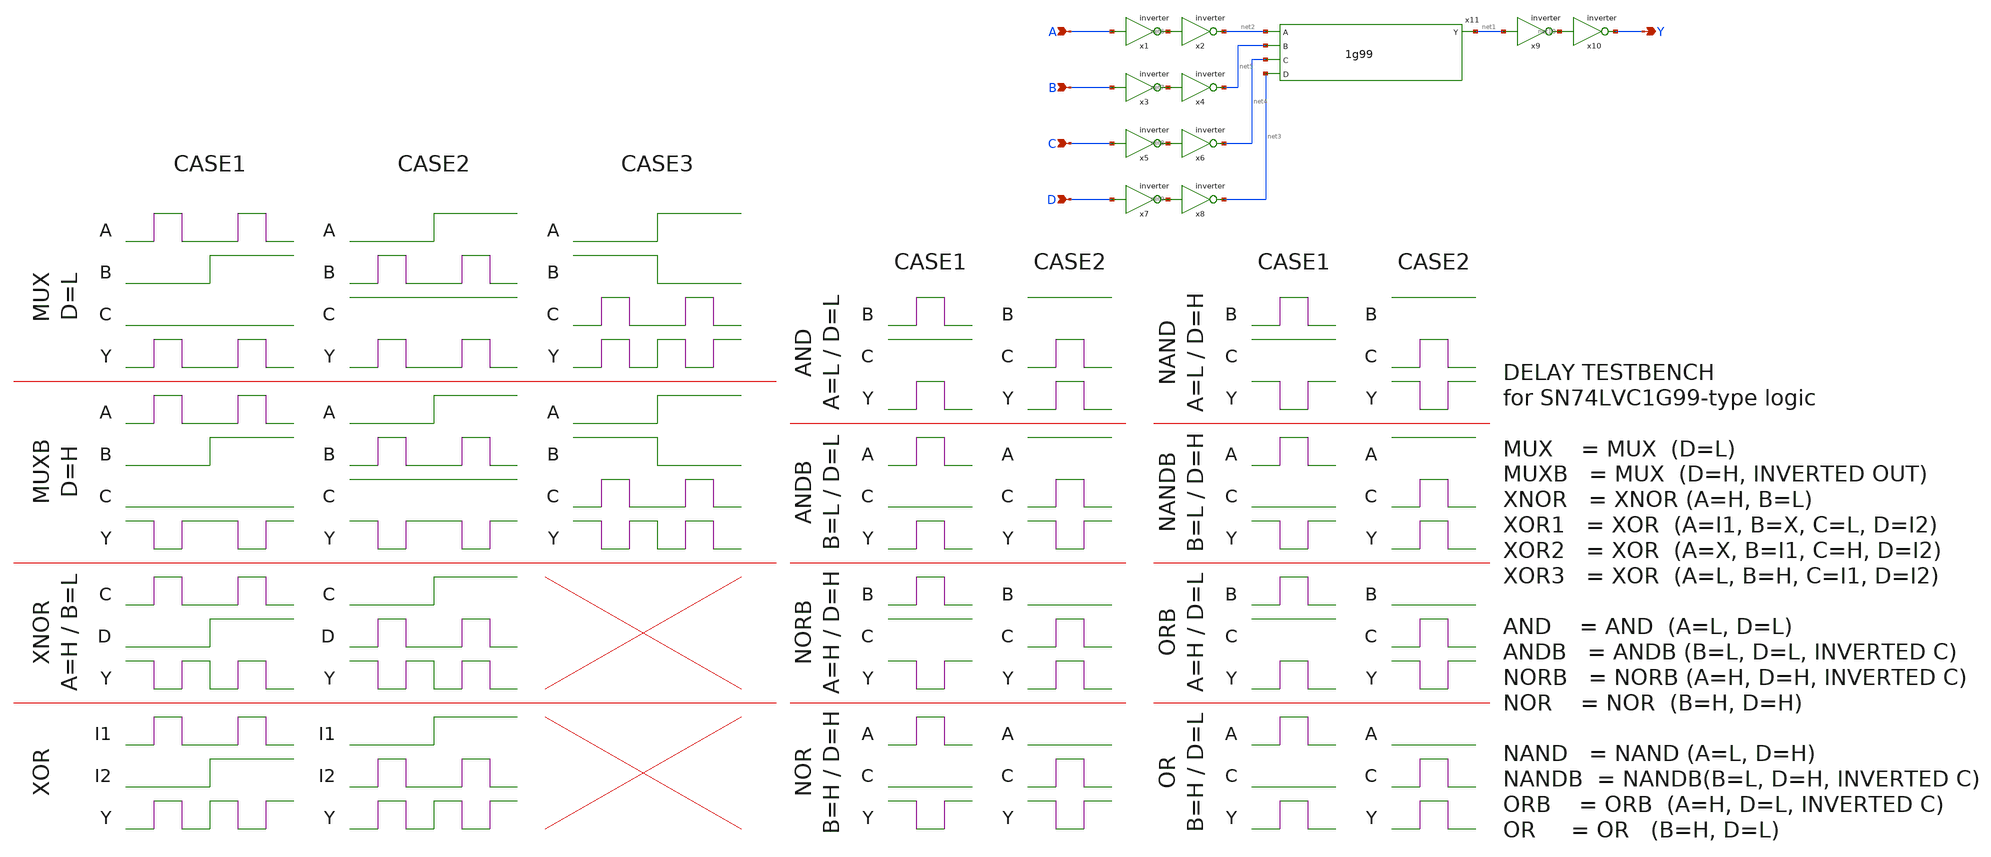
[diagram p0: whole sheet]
** sch_path: 1g99_delay2.sch
**.subckt 1g99_delay2 A B C D Y
*.ipin A
*.ipin B
*.ipin C
*.ipin D
*.opin Y
x1 net6 A inverter
x2 net2 net6 inverter
x3 net7 B inverter
x4 net5 net7 inverter
x5 net8 C inverter
x6 net4 net8 inverter
x7 net9 D inverter
x8 net3 net9 inverter
x9 net10 net1 inverter
x10 Y net10 inverter
x11 net2 net5 net1 net4 net3 1g99
**** begin user architecture code
 .param mc_mm_switch=0
.param mc_pr_switch=0
.include $::SKYWATER_MODELS/corners/tt.spice
.include $::SKYWATER_MODELS/r+c/res_typical__cap_typical.spice
.include $::SKYWATER_MODELS/r+c/res_typical__cap_typical__lin.spice
.include $::SKYWATER_MODELS/corners/tt/specialized_cells.spice
.include $::SKYWATER_STDCELLS/sky130_fd_sc_hd.spice




VP VDD 0 dc 1.8
VA A 0 dc 1.8
VB B 0 dc 1.8
VC C 0 dc 1.8
VD D 0 dc 1.8

.control
save a b c d y

// MUX AREA

alter @vd[PULSE] [ 0 0 10n 40p 40p 10n 30n ] // always L

alter @va[PULSE] [ 0 1.8 10n 40p 40p 10n 30n ]
alter @vb[PULSE] [ 0 1.8 30n 40p 40p 40n 80n ]
alter @vc[PULSE] [ 0 0 10n 40p 40p 10n 30n ]
tran 10p 60n
meas tran  in1 FIND time WHEN v(a)=0.9 RISE=1 > NUL
meas tran out1 FIND time WHEN v(y)=0.9 RISE=1 > NUL
meas tran  in2 FIND time WHEN v(a)=0.9 FALL=1 > NUL
meas tran out2 FIND time WHEN v(y)=0.9 FALL=1 > NUL
meas tran  in3 FIND time WHEN v(a)=0.9 RISE=2 > NUL
meas tran out3 FIND time WHEN v(y)=0.9 RISE=2 > NUL
meas tran  in4 FIND time WHEN v(a)=0.9 FALL=2 > NUL
meas tran out4 FIND time WHEN v(y)=0.9 FALL=2 > NUL

let calc1 = out1 - in1
set delay1 = $&calc1
let calc2 = out2 - in2
set delay2 = $&calc2
let calc3 = out3 - in3
set delay3 = $&calc3
let calc4 = out4 - in4
set delay4 = $&calc4

alter @vb[PULSE] [ 0 1.8 10n 40p 40p 10n 30n ]
alter @va[PULSE] [ 0 1.8 30n 40p 40p 40n 80n ]
alter @vc[PULSE] [ 1.8 1.8 10n 40p 40p 10n 30n ]
tran 10p 60n
meas tran  in5 FIND time WHEN v(b)=0.9 RISE=1 > NUL
meas tran out5 FIND time WHEN v(y)=0.9 RISE=1 > NUL
meas tran  in6 FIND time WHEN v(b)=0.9 FALL=1 > NUL
meas tran out6 FIND time WHEN v(y)=0.9 FALL=1 > NUL
meas tran  in7 FIND time WHEN v(b)=0.9 RISE=2 > NUL
meas tran out7 FIND time WHEN v(y)=0.9 RISE=2 > NUL
meas tran  in8 FIND time WHEN v(b)=0.9 FALL=2 > NUL
meas tran out8 FIND time WHEN v(y)=0.9 FALL=2 > NUL

let calc5 = out5 - in5
set delay5 = $&calc5
let calc6 = out6 - in6
set delay6 = $&calc6
let calc7 = out7 - in7
set delay7 = $&calc7
let calc8 = out8 - in8
set delay8 = $&calc8

alter @va[PULSE] [ 0 1.8 30n 40p 40p 40n 80n ]
alter @vb[PULSE] [ 1.8 0 30n 40p 40p 40n 80n ]
alter @vc[PULSE] [ 0 1.8 10n 40p 40p 10n 30n ]
tran 10p 60n
meas tran  in9 FIND time WHEN v(c)=0.9 RISE=1 > NUL
meas tran out9 FIND time WHEN v(y)=0.9 RISE=1 > NUL
meas tran  in10 FIND time WHEN v(c)=0.9 FALL=1 > NUL
meas tran out10 FIND time WHEN v(y)=0.9 FALL=1 > NUL
meas tran  in11 FIND time WHEN v(c)=0.9 RISE=2 > NUL
meas tran out11 FIND time WHEN v(y)=0.9 FALL=2 > NUL
meas tran  in12 FIND time WHEN v(c)=0.9 FALL=2 > NUL
meas tran out12 FIND time WHEN v(y)=0.9 RISE=3 > NUL

let calc9 = out9 - in9
set delay9 = $&calc9
let calc10 = out10 - in10
set delay10 = $&calc10
let calc11 = out11 - in11
set delay11 = $&calc11
let calc12 = out12 - in12
set delay12 = $&calc12

// MUXB AREA

alter @vd[PULSE] [ 1.8 1.8 10n 40p 40p 10n 30n ] // always H

alter @va[PULSE] [ 0 1.8 10n 40p 40p 10n 30n ]
alter @vb[PULSE] [ 0 1.8 30n 40p 40p 40n 80n ]
alter @vc[PULSE] [ 0 0 10n 40p 40p 10n 30n ]
tran 10p 60n
meas tran  in1 FIND time WHEN v(a)=0.9 RISE=1 > NUL
meas tran out1 FIND time WHEN v(y)=0.9 FALL=1 > NUL
meas tran  in2 FIND time WHEN v(a)=0.9 FALL=1 > NUL
meas tran out2 FIND time WHEN v(y)=0.9 RISE=1 > NUL
meas tran  in3 FIND time WHEN v(a)=0.9 RISE=2 > NUL
meas tran out3 FIND time WHEN v(y)=0.9 FALL=2 > NUL
meas tran  in4 FIND time WHEN v(a)=0.9 FALL=2 > NUL
meas tran out4 FIND time WHEN v(y)=0.9 RISE=2 > NUL

let calc1 = out1 - in1
set delayb1 = $&calc1
let calc2 = out2 - in2
set delayb2 = $&calc2
let calc3 = out3 - in3
set delayb3 = $&calc3
let calc4 = out4 - in4
set delayb4 = $&calc4

alter @vb[PULSE] [ 0 1.8 10n 40p 40p 10n 30n ]
alter @va[PULSE] [ 0 1.8 30n 40p 40p 40n 80n ]
alter @vc[PULSE] [ 1.8 1.8 10n 40p 40p 10n 30n ]
tran 10p 60n
meas tran  in5 FIND time WHEN v(b)=0.9 RISE=1 > NUL
meas tran out5 FIND time WHEN v(y)=0.9 FALL=1 > NUL
meas tran  in6 FIND time WHEN v(b)=0.9 FALL=1 > NUL
meas tran out6 FIND time WHEN v(y)=0.9 RISE=1 > NUL
meas tran  in7 FIND time WHEN v(b)=0.9 RISE=2 > NUL
meas tran out7 FIND time WHEN v(y)=0.9 FALL=2 > NUL
meas tran  in8 FIND time WHEN v(b)=0.9 FALL=2 > NUL
meas tran out8 FIND time WHEN v(y)=0.9 RISE=2 > NUL

let calc5 = out5 - in5
set delayb5 = $&calc5
let calc6 = out6 - in6
set delayb6 = $&calc6
let calc7 = out7 - in7
set delayb7 = $&calc7
let calc8 = out8 - in8
set delayb8 = $&calc8

alter @va[PULSE] [ 0 1.8 30n 40p 40p 40n 80n ]
alter @vb[PULSE] [ 1.8 0 30n 40p 40p 40n 80n ]
alter @vc[PULSE] [ 0 1.8 10n 40p 40p 10n 30n ]
tran 10p 60n
meas tran  in9 FIND time WHEN v(c)=0.9 RISE=1 > NUL
meas tran out9 FIND time WHEN v(y)=0.9 FALL=1 > NUL
meas tran  in10 FIND time WHEN v(c)=0.9 FALL=1 > NUL
meas tran out10 FIND time WHEN v(y)=0.9 RISE=1 > NUL
meas tran  in11 FIND time WHEN v(c)=0.9 RISE=2 > NUL
meas tran out11 FIND time WHEN v(y)=0.9 RISE=2 > NUL
meas tran  in12 FIND time WHEN v(c)=0.9 FALL=2 > NUL
meas tran out12 FIND time WHEN v(y)=0.9 FALL=3 > NUL

let calc9 = out9 - in9
set delayb9 = $&calc9
let calc10 = out10 - in10
set delayb10 = $&calc10
let calc11 = out11 - in11
set delayb11 = $&calc11
let calc12 = out12 - in12
set delayb12 = $&calc12

// XNOR AREA

alter @va[PULSE] [ 1.8 1.8 30n 40p 40p 10n 30n ] // always H
alter @vb[PULSE] [ 0 0 30n 40p 40p 10n 30n ] // always L
alter @vc[PULSE] [ 0 1.8 10n 40p 40p 10n 30n ]
alter @vd[PULSE] [ 0 1.8 30n 40p 40p 40n 80n ]
tran 10p 60n
meas tran  in1 FIND time WHEN v(c)=0.9 RISE=1 > NUL
meas tran out1 FIND time WHEN v(y)=0.9 FALL=1 > NUL
meas tran  in2 FIND time WHEN v(c)=0.9 FALL=1 > NUL
meas tran out2 FIND time WHEN v(y)=0.9 RISE=1 > NUL
meas tran  in3 FIND time WHEN v(c)=0.9 RISE=2 > NUL
meas tran out3 FIND time WHEN v(y)=0.9 RISE=2 > NUL
meas tran  in4 FIND time WHEN v(c)=0.9 FALL=2 > NUL
meas tran out4 FIND time WHEN v(y)=0.9 FALL=3 > NUL

let calc1 = out1 - in1
set delayxn1 = $&calc1
let calc2 = out2 - in2
set delayxn2 = $&calc2
let calc3 = out3 - in3
set delayxn3 = $&calc3
let calc4 = out4 - in4
set delayxn4 = $&calc4

alter @vd[PULSE] [ 0 1.8 10n 40p 40p 10n 30n ]
alter @vc[PULSE] [ 0 1.8 30n 40p 40p 40n 80n ]
tran 10p 60n
meas tran  in5 FIND time WHEN v(d)=0.9 RISE=1 > NUL
meas tran out5 FIND time WHEN v(y)=0.9 FALL=1 > NUL
meas tran  in6 FIND time WHEN v(d)=0.9 FALL=1 > NUL
meas tran out6 FIND time WHEN v(y)=0.9 RISE=1 > NUL
meas tran  in7 FIND time WHEN v(d)=0.9 RISE=2 > NUL
meas tran out7 FIND time WHEN v(y)=0.9 RISE=2 > NUL
meas tran  in8 FIND time WHEN v(d)=0.9 FALL=2 > NUL
meas tran out8 FIND time WHEN v(y)=0.9 FALL=3 > NUL

let calc5 = out5 - in5
set delayxn5 = $&calc5
let calc6 = out6 - in6
set delayxn6 = $&calc6
let calc7 = out7 - in7
set delayxn7 = $&calc7
let calc8 = out8 - in8
set delayxn8 = $&calc8

// XOR_A AREA

alter @vb[PULSE] [ 0 0 10n 40p 40p 10n 30n ] // assume L
alter @vc[PULSE] [ 0 0 10n 40p 40p 10n 30n ] // always L

alter @va[PULSE] [ 0 1.8 10n 40p 40p 10n 30n ]
alter @vd[PULSE] [ 0 1.8 30n 40p 40p 40n 80n ]
tran 10p 60n
meas tran  in1 FIND time WHEN v(a)=0.9 RISE=1 > NUL
meas tran out1 FIND time WHEN v(y)=0.9 RISE=1 > NUL
meas tran  in2 FIND time WHEN v(a)=0.9 FALL=1 > NUL
meas tran out2 FIND time WHEN v(y)=0.9 FALL=1 > NUL
meas tran  in3 FIND time WHEN v(a)=0.9 RISE=2 > NUL
meas tran out3 FIND time WHEN v(y)=0.9 FALL=2 > NUL
meas tran  in4 FIND time WHEN v(a)=0.9 FALL=2 > NUL
meas tran out4 FIND time WHEN v(y)=0.9 RISE=3 > NUL

let calc1 = out1 - in1
set delayxa1 = $&calc1
let calc2 = out2 - in2
set delayxa2 = $&calc2
let calc3 = out3 - in3
set delayxa3 = $&calc3
let calc4 = out4 - in4
set delayxa4 = $&calc4

alter @vd[PULSE] [ 0 1.8 10n 40p 40p 10n 30n ]
alter @va[PULSE] [ 0 1.8 30n 40p 40p 40n 80n ]
tran 10p 60n
meas tran  in5 FIND time WHEN v(d)=0.9 RISE=1 > NUL
meas tran out5 FIND time WHEN v(y)=0.9 RISE=1 > NUL
meas tran  in6 FIND time WHEN v(d)=0.9 FALL=1 > NUL
meas tran out6 FIND time WHEN v(y)=0.9 FALL=1 > NUL
meas tran  in7 FIND time WHEN v(d)=0.9 RISE=2 > NUL
meas tran out7 FIND time WHEN v(y)=0.9 FALL=2 > NUL
meas tran  in8 FIND time WHEN v(d)=0.9 FALL=2 > NUL
meas tran out8 FIND time WHEN v(y)=0.9 RISE=3 > NUL

let calc5 = out5 - in5
set delayxa5 = $&calc5
let calc6 = out6 - in6
set delayxa6 = $&calc6
let calc7 = out7 - in7
set delayxa7 = $&calc7
let calc8 = out8 - in8
set delayxa8 = $&calc8

// XOR_B AREA

alter @va[PULSE] [ 0 0 10n 40p 40p 10n 30n ]     // assume L
alter @vc[PULSE] [ 1.8 1.8 10n 40p 40p 10n 30n ] // always H

alter @vb[PULSE] [ 0 1.8 10n 40p 40p 10n 30n ]
alter @vd[PULSE] [ 0 1.8 30n 40p 40p 40n 80n ]
tran 10p 60n
meas tran  in1 FIND time WHEN v(b)=0.9 RISE=1 > NUL
meas tran out1 FIND time WHEN v(y)=0.9 RISE=1 > NUL
meas tran  in2 FIND time WHEN v(b)=0.9 FALL=1 > NUL
meas tran out2 FIND time WHEN v(y)=0.9 FALL=1 > NUL
meas tran  in3 FIND time WHEN v(b)=0.9 RISE=2 > NUL
meas tran out3 FIND time WHEN v(y)=0.9 FALL=2 > NUL
meas tran  in4 FIND time WHEN v(b)=0.9 FALL=2 > NUL
meas tran out4 FIND time WHEN v(y)=0.9 RISE=3 > NUL

let calc1 = out1 - in1
set delayxb1 = $&calc1
let calc2 = out2 - in2
set delayxb2 = $&calc2
let calc3 = out3 - in3
set delayxb3 = $&calc3
let calc4 = out4 - in4
set delayxb4 = $&calc4

alter @vd[PULSE] [ 0 1.8 10n 40p 40p 10n 30n ]
alter @vb[PULSE] [ 0 1.8 30n 40p 40p 40n 80n ]
tran 10p 60n
meas tran  in5 FIND time WHEN v(d)=0.9 RISE=1 > NUL
meas tran out5 FIND time WHEN v(y)=0.9 RISE=1 > NUL
meas tran  in6 FIND time WHEN v(d)=0.9 FALL=1 > NUL
meas tran out6 FIND time WHEN v(y)=0.9 FALL=1 > NUL
meas tran  in7 FIND time WHEN v(d)=0.9 RISE=2 > NUL
meas tran out7 FIND time WHEN v(y)=0.9 FALL=2 > NUL
meas tran  in8 FIND time WHEN v(d)=0.9 FALL=2 > NUL
meas tran out8 FIND time WHEN v(y)=0.9 RISE=3 > NUL

let calc5 = out5 - in5
set delayxb5 = $&calc5
let calc6 = out6 - in6
set delayxb6 = $&calc6
let calc7 = out7 - in7
set delayxb7 = $&calc7
let calc8 = out8 - in8
set delayxb8 = $&calc8

//XOR_C AREA

alter @va[PULSE] [ 0 0 10n 40p 40p 10n 30n ]     // assume L
alter @vb[PULSE] [ 1.8 1.8 10n 40p 40p 10n 30n ] // always H

alter @vc[PULSE] [ 0 1.8 10n 40p 40p 10n 30n ]
alter @vd[PULSE] [ 0 1.8 30n 40p 40p 40n 80n ]
tran 10p 60n
meas tran  in1 FIND time WHEN v(c)=0.9 RISE=1 > NUL
meas tran out1 FIND time WHEN v(y)=0.9 RISE=1 > NUL
meas tran  in2 FIND time WHEN v(c)=0.9 FALL=1 > NUL
meas tran out2 FIND time WHEN v(y)=0.9 FALL=1 > NUL
meas tran  in3 FIND time WHEN v(c)=0.9 RISE=2 > NUL
meas tran out3 FIND time WHEN v(y)=0.9 FALL=2 > NUL
meas tran  in4 FIND time WHEN v(c)=0.9 FALL=2 > NUL
meas tran out4 FIND time WHEN v(y)=0.9 RISE=3 > NUL

let calc1 = out1 - in1
set delayxc1 = $&calc1
let calc2 = out2 - in2
set delayxc2 = $&calc2
let calc3 = out3 - in3
set delayxc3 = $&calc3
let calc4 = out4 - in4
set delayxc4 = $&calc4

alter @vd[PULSE] [ 0 1.8 10n 40p 40p 10n 30n ]
alter @vc[PULSE] [ 0 1.8 30n 40p 40p 40n 80n ]
tran 10p 60n
meas tran  in5 FIND time WHEN v(d)=0.9 RISE=1 > NUL
meas tran out5 FIND time WHEN v(y)=0.9 RISE=1 > NUL
meas tran  in6 FIND time WHEN v(d)=0.9 FALL=1 > NUL
meas tran out6 FIND time WHEN v(y)=0.9 FALL=1 > NUL
meas tran  in7 FIND time WHEN v(d)=0.9 RISE=2 > NUL
meas tran out7 FIND time WHEN v(y)=0.9 FALL=2 > NUL
meas tran  in8 FIND time WHEN v(d)=0.9 FALL=2 > NUL
meas tran out8 FIND time WHEN v(y)=0.9 RISE=3 > NUL

let calc5 = out5 - in5
set delayxc5 = $&calc5
let calc6 = out6 - in6
set delayxc6 = $&calc6
let calc7 = out7 - in7
set delayxc7 = $&calc7
let calc8 = out8 - in8
set delayxc8 = $&calc8

// AND AREA

alter @va[PULSE] [ 0 0 10n 40p 40p 10n 30n ] // always L
alter @vd[PULSE] [ 0 0 10n 40p 40p 10n 30n ] // always L

alter @vb[PULSE] [ 0 1.8 10n 40p 40p 10n 30n ]
alter @vc[PULSE] [ 1.8 1.8 10n 40p 40p 10n 30n ]
tran 10p 30n
meas tran  in1 FIND time WHEN v(b)=0.9 RISE=1 > NUL
meas tran out1 FIND time WHEN v(y)=0.9 RISE=1 > NUL
meas tran  in2 FIND time WHEN v(b)=0.9 FALL=1 > NUL
meas tran out2 FIND time WHEN v(y)=0.9 FALL=1 > NUL

let calc1 = out1 - in1
set delaya1 = $&calc1
let calc2 = out2 - in2
set delaya2 = $&calc2

alter @vc[PULSE] [ 0 1.8 10n 40p 40p 10n 30n ]
alter @vb[PULSE] [ 1.8 1.8 10n 40p 40p 10n 30n ]
tran 10p 30n
meas tran  in5 FIND time WHEN v(c)=0.9 RISE=1 > NUL
meas tran out5 FIND time WHEN v(y)=0.9 RISE=1 > NUL
meas tran  in6 FIND time WHEN v(c)=0.9 FALL=1 > NUL
meas tran out6 FIND time WHEN v(y)=0.9 FALL=1 > NUL

let calc5 = out5 - in5
set delaya5 = $&calc5
let calc6 = out6 - in6
set delaya6 = $&calc6

// NORB_A AREA

alter @vb[PULSE] [ 0 0 10n 40p 40p 10n 30n ] // always L
alter @vd[PULSE] [ 0 0 10n 40p 40p 10n 30n ] // always L

alter @va[PULSE] [ 0 1.8 10n 40p 40p 10n 30n ]
alter @vc[PULSE] [ 0 0 10n 40p 40p 10n 30n ]
tran 10p 30n
meas tran  in1 FIND time WHEN v(a)=0.9 RISE=1 > NUL
meas tran out1 FIND time WHEN v(y)=0.9 RISE=1 > NUL
meas tran  in2 FIND time WHEN v(a)=0.9 FALL=1 > NUL
meas tran out2 FIND time WHEN v(y)=0.9 FALL=1 > NUL

let calc1 = out1 - in1
set delayab1 = $&calc1
let calc2 = out2 - in2
set delayab2 = $&calc2

alter @vc[PULSE] [ 0 1.8 10n 40p 40p 10n 30n ]
alter @va[PULSE] [ 1.8 1.8 10n 40p 40p 10n 30n ]
tran 10p 30n
meas tran  in5 FIND time WHEN v(c)=0.9 RISE=1 > NUL
meas tran out5 FIND time WHEN v(y)=0.9 FALL=1 > NUL
meas tran  in6 FIND time WHEN v(c)=0.9 FALL=1 > NUL
meas tran out6 FIND time WHEN v(y)=0.9 RISE=1 > NUL

let calc5 = out5 - in5
set delayab5 = $&calc5
let calc6 = out6 - in6
set delayab6 = $&calc6

// NORB_B AREA

alter @vb[PULSE] [ 1.8 1.8 10n 40p 40p 10n 30n ] // always H
alter @vd[PULSE] [ 1.8 1.8 10n 40p 40p 10n 30n ] // always H

alter @vb[PULSE] [ 0 1.8 10n 40p 40p 10n 30n ]
alter @vc[PULSE] [ 1.8 1.8 10n 40p 40p 10n 30n ]
tran 10p 30n
meas tran  in1 FIND time WHEN v(b)=0.9 RISE=1 > NUL
meas tran out1 FIND time WHEN v(y)=0.9 FALL=1 > NUL
meas tran  in2 FIND time WHEN v(b)=0.9 FALL=1 > NUL
meas tran out2 FIND time WHEN v(y)=0.9 RISE=1 > NUL

let calc1 = out1 - in1
set delaynob1 = $&calc1
let calc2 = out2 - in2
set delaynob2 = $&calc2

alter @vc[PULSE] [ 0 1.8 10n 40p 40p 10n 30n ]
alter @vb[PULSE] [ 0 0 10n 40p 40p 10n 30n ]
tran 10p 30n
meas tran  in5 FIND time WHEN v(c)=0.9 RISE=1 > NUL
meas tran out5 FIND time WHEN v(y)=0.9 RISE=1 > NUL
meas tran  in6 FIND time WHEN v(c)=0.9 FALL=1 > NUL
meas tran out6 FIND time WHEN v(y)=0.9 FALL=1 > NUL

let calc5 = out5 - in5
set delaynob5 = $&calc5
let calc6 = out6 - in6
set delaynob6 = $&calc6


// NOR AREA

alter @vb[PULSE] [ 1.8 1.8 10n 40p 40p 10n 30n ] // always H
alter @vd[PULSE] [ 1.8 1.8 10n 40p 40p 10n 30n ] // always H

alter @va[PULSE] [ 0 1.8 10n 40p 40p 10n 30n ]
alter @vc[PULSE] [ 0 0 10n 40p 40p 10n 30n ]
tran 10p 30n
meas tran  in1 FIND time WHEN v(a)=0.9 RISE=1 > NUL
meas tran out1 FIND time WHEN v(y)=0.9 FALL=1 > NUL
meas tran  in2 FIND time WHEN v(a)=0.9 FALL=1 > NUL
meas tran out2 FIND time WHEN v(y)=0.9 RISE=1 > NUL

let calc1 = out1 - in1
set delayno1 = $&calc1
let calc2 = out2 - in2
set delayno2 = $&calc2

alter @vc[PULSE] [ 0 1.8 10n 40p 40p 10n 30n ]
alter @va[PULSE] [ 0 0 10n 40p 40p 10n 30n ]
tran 10p 30n
meas tran  in5 FIND time WHEN v(c)=0.9 RISE=1 > NUL
meas tran out5 FIND time WHEN v(y)=0.9 FALL=1 > NUL
meas tran  in6 FIND time WHEN v(c)=0.9 FALL=1 > NUL
meas tran out6 FIND time WHEN v(y)=0.9 RISE=1 > NUL

let calc5 = out5 - in5
set delayno5 = $&calc5
let calc6 = out6 - in6
set delayno6 = $&calc6

// NAND AREA

alter @va[PULSE] [ 0 0 10n 40p 40p 10n 30n ]     // always L
alter @vd[PULSE] [ 1.8 1.8 10n 40p 40p 10n 30n ] // always H

alter @vb[PULSE] [ 0 1.8 10n 40p 40p 10n 30n ]
alter @vc[PULSE] [ 1.8 1.8 10n 40p 40p 10n 30n ]
tran 10p 30n
meas tran  in1 FIND time WHEN v(b)=0.9 RISE=1 > NUL
meas tran out1 FIND time WHEN v(y)=0.9 FALL=1 > NUL
meas tran  in2 FIND time WHEN v(b)=0.9 FALL=1 > NUL
meas tran out2 FIND time WHEN v(y)=0.9 RISE=1 > NUL

let calc1 = out1 - in1
set delayna1 = $&calc1
let calc2 = out2 - in2
set delayna2 = $&calc2

alter @vc[PULSE] [ 0 1.8 10n 40p 40p 10n 30n ]
alter @vb[PULSE] [ 1.8 1.8 10n 40p 40p 10n 30n ]
tran 10p 30n
meas tran  in5 FIND time WHEN v(c)=0.9 RISE=1 > NUL
meas tran out5 FIND time WHEN v(y)=0.9 FALL=1 > NUL
meas tran  in6 FIND time WHEN v(c)=0.9 FALL=1 > NUL
meas tran out6 FIND time WHEN v(y)=0.9 RISE=1 > NUL

let calc5 = out5 - in5
set delayna5 = $&calc5
let calc6 = out6 - in6
set delayna6 = $&calc6

// NANDB_A AREA

alter @vb[PULSE] [ 0 0 10n 40p 40p 10n 30n ]     // always L
alter @vd[PULSE] [ 1.8 1.8 10n 40p 40p 10n 30n ] // always H

alter @va[PULSE] [ 0 1.8 10n 40p 40p 10n 30n ]
alter @vc[PULSE] [ 0 0 10n 40p 40p 10n 30n ]
tran 10p 30n
meas tran  in1 FIND time WHEN v(a)=0.9 RISE=1 > NUL
meas tran out1 FIND time WHEN v(y)=0.9 FALL=1 > NUL
meas tran  in2 FIND time WHEN v(a)=0.9 FALL=1 > NUL
meas tran out2 FIND time WHEN v(y)=0.9 RISE=1 > NUL

let calc1 = out1 - in1
set delaynab1 = $&calc1
let calc2 = out2 - in2
set delaynab2 = $&calc2

alter @vc[PULSE] [ 0 1.8 10n 40p 40p 10n 30n ]
alter @va[PULSE] [ 1.8 1.8 10n 40p 40p 10n 30n ]
tran 10p 30n
meas tran  in5 FIND time WHEN v(c)=0.9 RISE=1 > NUL
meas tran out5 FIND time WHEN v(y)=0.9 RISE=1 > NUL
meas tran  in6 FIND time WHEN v(c)=0.9 FALL=1 > NUL
meas tran out6 FIND time WHEN v(y)=0.9 FALL=1 > NUL

let calc5 = out5 - in5
set delaynab5 = $&calc5
let calc6 = out6 - in6
set delaynab6 = $&calc6

// NANDB_B AREA

alter @va[PULSE] [ 1.8 1.8 10n 40p 40p 10n 30n ] // always H
alter @vd[PULSE] [ 0 0 10n 40p 40p 10n 30n ]     // always L

alter @vb[PULSE] [ 0 1.8 10n 40p 40p 10n 30n ]
alter @vc[PULSE] [ 1.8 1.8 10n 40p 40p 10n 30n ]
tran 10p 30n
meas tran  in1 FIND time WHEN v(b)=0.9 RISE=1 > NUL
meas tran out1 FIND time WHEN v(y)=0.9 RISE=1 > NUL
meas tran  in2 FIND time WHEN v(b)=0.9 FALL=1 > NUL
meas tran out2 FIND time WHEN v(y)=0.9 FALL=1 > NUL

let calc1 = out1 - in1
set delayob1 = $&calc1
let calc2 = out2 - in2
set delayob2 = $&calc2

alter @vc[PULSE] [ 0 1.8 10n 40p 40p 10n 30n ]
alter @vb[PULSE] [ 0 0 10n 40p 40p 10n 30n ]
tran 10p 30n
meas tran  in5 FIND time WHEN v(c)=0.9 RISE=1 > NUL
meas tran out5 FIND time WHEN v(y)=0.9 FALL=1 > NUL
meas tran  in6 FIND time WHEN v(c)=0.9 FALL=1 > NUL
meas tran out6 FIND time WHEN v(y)=0.9 RISE=1 > NUL

let calc5 = out5 - in5
set delayob5 = $&calc5
let calc6 = out6 - in6
set delayob6 = $&calc6

// OR AREA

alter @vb[PULSE] [ 1.8 1.8 10n 40p 40p 10n 30n ] // always H
alter @vd[PULSE] [ 0 0 10n 40p 40p 10n 30n ]     // always L

alter @va[PULSE] [ 0 1.8 10n 40p 40p 10n 30n ]
alter @vc[PULSE] [ 0 0 10n 40p 40p 10n 30n ]
tran 10p 30n
meas tran  in1 FIND time WHEN v(a)=0.9 RISE=1 > NUL
meas tran out1 FIND time WHEN v(y)=0.9 RISE=1 > NUL
meas tran  in2 FIND time WHEN v(a)=0.9 FALL=1 > NUL
meas tran out2 FIND time WHEN v(y)=0.9 FALL=1 > NUL

let calc1 = out1 - in1
set delayo1 = $&calc1
let calc2 = out2 - in2
set delayo2 = $&calc2

alter @vc[PULSE] [ 0 1.8 10n 40p 40p 10n 30n ]
alter @va[PULSE] [ 0 0 10n 40p 40p 10n 30n ]
tran 10p 30n
meas tran  in5 FIND time WHEN v(c)=0.9 RISE=1 > NUL
meas tran out5 FIND time WHEN v(y)=0.9 RISE=1 > NUL
meas tran  in6 FIND time WHEN v(c)=0.9 FALL=1 > NUL
meas tran out6 FIND time WHEN v(y)=0.9 FALL=1 > NUL

let calc5 = out5 - in5
set delayo5 = $&calc5
let calc6 = out6 - in6
set delayo6 = $&calc6

// ECHO RESULTS

echo '*** MUX DELAY CASE 1 ***'
echo 'A(LH) when B(L)&C(L) ='{$delay1}
echo 'A(HL) when B(L)&C(L) ='{$delay2}
echo 'A(LH) when B(H)&C(L) ='{$delay3}
echo 'A(HL) when B(H)&C(L) ='{$delay4}

echo '*** MUX DELAY CASE 2 ***'
echo 'B(LH) when A(L)&C(L) ='{$delay5}
echo 'B(HL) when A(L)&C(L) ='{$delay6}
echo 'B(LH) when A(H)&C(L) ='{$delay7}
echo 'B(HL) when A(H)&C(L) ='{$delay8}

echo '*** MUX DELAY CASE 3 ***'
echo 'C(LH) when A(L)&B(H) ='{$delay9}
echo 'C(HL) when A(L)&B(H) ='{$delay10}
echo 'C(LH) when A(H)&B(L) ='{$delay11}
echo 'C(HL) when A(H)&B(L) ='{$delay12}

echo '*** MUXB DELAY CASE 1 ***'
echo 'A(LH) when B(L)&C(L) ='{$delayb1}
echo 'A(HL) when B(L)&C(L) ='{$delayb2}
echo 'A(LH) when B(H)&C(L) ='{$delayb3}
echo 'A(HL) when B(H)&C(L) ='{$delayb4}

echo '*** MUXB DELAY CASE 2 ***'
echo 'B(LH) when A(L)&C(L) ='{$delayb5}
echo 'B(HL) when A(L)&C(L) ='{$delayb6}
echo 'B(LH) when A(H)&C(L) ='{$delayb7}
echo 'B(HL) when A(H)&C(L) ='{$delayb8}

echo '*** MUXB DELAY CASE 3 ***'
echo 'C(LH) when A(L)&B(H) ='{$delayb9}
echo 'C(HL) when A(L)&B(H) ='{$delayb10}
echo 'C(LH) when A(H)&B(L) ='{$delayb11}
echo 'C(HL) when A(H)&B(L) ='{$delayb12}

echo '*** XNOR DELAY CASE 1 ***'
echo 'C(LH) when D(L) ='{$delayxn1}
echo 'C(HL) when D(L) ='{$delayxn2}
echo 'C(LH) when D(H) ='{$delayxn3}
echo 'C(HL) when D(H) ='{$delayxn4}

echo '*** XNOR DELAY CASE 2 ***'
echo 'D(LH) when C(L) ='{$delayxn5}
echo 'D(HL) when C(L) ='{$delayxn6}
echo 'D(LH) when C(H) ='{$delayxn7}
echo 'D(HL) when C(H) ='{$delayxn8}

echo '*** XOR1 DELAY CASE 1 ***'
echo 'A(LH) when D(L) ='{$delayxa1}
echo 'A(HL) when D(L) ='{$delayxa2}
echo 'A(LH) when D(H) ='{$delayxa3}
echo 'A(HL) when D(H) ='{$delayxa4}

echo '*** XOR1 DELAY CASE 2 ***'
echo 'D(LH) when A(L) ='{$delayxa5}
echo 'D(HL) when A(L) ='{$delayxa6}
echo 'D(LH) when A(H) ='{$delayxa7}
echo 'D(HL) when A(H) ='{$delayxa8}

echo '*** XOR2 DELAY CASE 1 ***'
echo 'B(LH) when D(L) ='{$delayxb1}
echo 'B(HL) when D(L) ='{$delayxb2}
echo 'B(LH) when D(H) ='{$delayxb3}
echo 'B(HL) when D(H) ='{$delayxb4}

echo '*** XOR2 DELAY CASE 2 ***'
echo 'D(LH) when B(L) ='{$delayxb5}
echo 'D(HL) when B(L) ='{$delayxb6}
echo 'D(LH) when B(H) ='{$delayxb7}
echo 'D(HL) when B(H) ='{$delayxb8}

echo '*** XOR3 DELAY CASE 1 ***'
echo 'C(LH) when D(L) ='{$delayxc1}
echo 'C(HL) when D(L) ='{$delayxc2}
echo 'C(LH) when D(H) ='{$delayxc3}
echo 'C(HL) when D(H) ='{$delayxc4}

echo '*** XOR3 DELAY CASE 2 ***'
echo 'D(LH) when C(L) ='{$delayxc5}
echo 'D(HL) when C(L) ='{$delayxc6}
echo 'D(LH) when C(H) ='{$delayxc7}
echo 'D(HL) when C(H) ='{$delayxc8}

echo '*** AND DELAY CASE 1 ***'
echo 'B(LH) when C(H) ='{$delaya1}
echo 'B(HL) when C(H) ='{$delaya2}

echo '*** AND DELAY CASE 2 ***'
echo 'C(LH) when B(L) ='{$delaya5}
echo 'C(HL) when B(L) ='{$delaya6}

echo '*** ANDB DELAY CASE 1 ***'
echo 'A(LH) when C(L) ='{$delayab1}
echo 'A(HL) when C(L) ='{$delayab2}

echo '*** ANDB DELAY CASE 2 ***'
echo 'C(LH) when A(H) ='{$delayab5}
echo 'C(HL) when A(H) ='{$delayab6}

echo '*** NORB DELAY CASE 1 ***'
echo 'B(LH) when C(H) ='{$delaynob1}
echo 'B(HL) when C(H) ='{$delaynob2}

echo '*** NORB DELAY CASE 2 ***'
echo 'C(LH) when B(L) ='{$delaynob5}
echo 'C(HL) when B(L) ='{$delaynob6}

echo '*** NOR DELAY CASE 1 ***'
echo 'A(LH) when C(L) ='{$delayno1}
echo 'A(HL) when C(L) ='{$delayno2}

echo '*** NOR DELAY CASE 2 ***'
echo 'C(LH) when A(L) ='{$delayno5}
echo 'C(HL) when A(L) ='{$delayno6}

echo '*** NAND DELAY CASE 1 ***'
echo 'B(LH) when C(H) ='{$delayna1}
echo 'B(HL) when C(H) ='{$delayna2}

echo '*** NAND DELAY CASE 2 ***'
echo 'C(LH) when B(H) ='{$delayna5}
echo 'C(HL) when B(H) ='{$delayna6}

echo '*** NANDB DELAY CASE 1 ***'
echo 'A(LH) when C(L) ='{$delaynab1}
echo 'A(HL) when C(L) ='{$delaynab2}

echo '*** NANDB DELAY CASE 2 ***'
echo 'C(LH) when A(H) ='{$delaynab5}
echo 'C(HL) when A(H) ='{$delaynab6}

echo '*** ORB DELAY CASE 1 ***'
echo 'B(LH) when C(H) ='{$delayob1}
echo 'B(HL) when C(H) ='{$delayob2}

echo '*** ORB DELAY CASE 2 ***'
echo 'C(LH) when B(L) ='{$delayob5}
echo 'C(HL) when B(L) ='{$delayob6}

echo '*** OR DELAY CASE 1 ***'
echo 'A(LH) when C(L) ='{$delayo1}
echo 'A(HL) when C(L) ='{$delayo2}

echo '*** OR DELAY CASE 2 ***'
echo 'C(LH) when A(L) ='{$delayo5}
echo 'C(HL) when A(L) ='{$delayo6}
.endc



**** end user architecture code
**.ends

* expanding   symbol:  inverter.sym # of pins=2
** sym_path: inverter.sym
** sch_path: inverter.sch
.subckt inverter Y A
*.ipin A
*.opin Y
XM1 Y A VDD VDD sky130_fd_pr__pfet_01v8 L=0.15 W=2.2 nf=1 ad='int((nf+1)/2) * W/nf * 0.29' as='int((nf+2)/2) * W/nf * 0.29'
+ pd='2*int((nf+1)/2) * (W/nf + 0.29)' ps='2*int((nf+2)/2) * (W/nf + 0.29)' nrd='0.29 / W' nrs='0.29 / W'
+ sa=0 sb=0 sd=0 mult=1 m=1
XM2 Y A GND GND sky130_fd_pr__nfet_01v8 L=0.15 W=1 nf=1 ad='int((nf+1)/2) * W/nf * 0.29' as='int((nf+2)/2) * W/nf * 0.29'
+ pd='2*int((nf+1)/2) * (W/nf + 0.29)' ps='2*int((nf+2)/2) * (W/nf + 0.29)' nrd='0.29 / W' nrs='0.29 / W'
+ sa=0 sb=0 sd=0 mult=1 m=1
.ends


* expanding   symbol:  1g99.sym # of pins=5
** sym_path: 1g99.sym
** sch_path: 1g99.sch
.subckt 1g99 A B Y C D
*.ipin A
*.ipin B
*.ipin C
*.ipin D
*.opin Y
.ends

.GLOBAL GND
.GLOBAL VDD
.end
